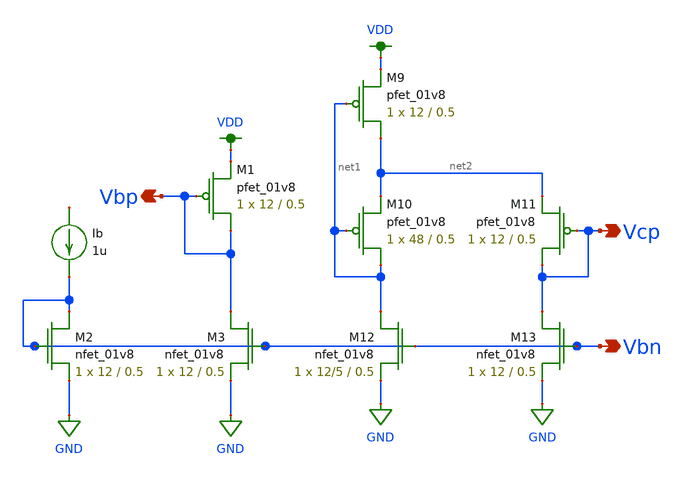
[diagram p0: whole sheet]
** sch_path: simulation/dac/cascode_v_gen.sch
**.subckt cascode_v_gen Vbn Vcp Vbp
*.opin Vbn
*.opin Vcp
*.opin Vbp
XM1 Vbp Vbp VDD VDD sky130_fd_pr__pfet_01v8 L=0.5 W=12 nf=1 ad='int((nf+1)/2) * W/nf * 0.29' as='int((nf+2)/2) * W/nf * 0.29'
+ pd='2*int((nf+1)/2) * (W/nf + 0.29)' ps='2*int((nf+2)/2) * (W/nf + 0.29)' nrd='0.29 / W' nrs='0.29 / W'
+ sa=0 sb=0 sd=0 mult=1 m=1
XM2 Vbn Vbn GND GND sky130_fd_pr__nfet_01v8 L=0.5 W=12 nf=1 ad='int((nf+1)/2) * W/nf * 0.29' as='int((nf+2)/2) * W/nf * 0.29'
+ pd='2*int((nf+1)/2) * (W/nf + 0.29)' ps='2*int((nf+2)/2) * (W/nf + 0.29)' nrd='0.29 / W' nrs='0.29 / W'
+ sa=0 sb=0 sd=0 mult=1 m=1
XM3 Vbp Vbn GND GND sky130_fd_pr__nfet_01v8 L=0.5 W=12 nf=1 ad='int((nf+1)/2) * W/nf * 0.29' as='int((nf+2)/2) * W/nf * 0.29'
+ pd='2*int((nf+1)/2) * (W/nf + 0.29)' ps='2*int((nf+2)/2) * (W/nf + 0.29)' nrd='0.29 / W' nrs='0.29 / W'
+ sa=0 sb=0 sd=0 mult=1 m=1
XM9 net2 net1 VDD VDD sky130_fd_pr__pfet_01v8 L=0.5 W=12 nf=1 ad='int((nf+1)/2) * W/nf * 0.29' as='int((nf+2)/2) * W/nf * 0.29'
+ pd='2*int((nf+1)/2) * (W/nf + 0.29)' ps='2*int((nf+2)/2) * (W/nf + 0.29)' nrd='0.29 / W' nrs='0.29 / W'
+ sa=0 sb=0 sd=0 mult=1 m=1
XM10 net1 net1 net2 VDD sky130_fd_pr__pfet_01v8 L=0.5 W=48 nf=1 ad='int((nf+1)/2) * W/nf * 0.29' as='int((nf+2)/2) * W/nf * 0.29'
+ pd='2*int((nf+1)/2) * (W/nf + 0.29)' ps='2*int((nf+2)/2) * (W/nf + 0.29)' nrd='0.29 / W' nrs='0.29 / W'
+ sa=0 sb=0 sd=0 mult=1 m=1
XM11 Vcp Vcp net2 VDD sky130_fd_pr__pfet_01v8 L=0.5 W=12 nf=1 ad='int((nf+1)/2) * W/nf * 0.29' as='int((nf+2)/2) * W/nf * 0.29'
+ pd='2*int((nf+1)/2) * (W/nf + 0.29)' ps='2*int((nf+2)/2) * (W/nf + 0.29)' nrd='0.29 / W' nrs='0.29 / W'
+ sa=0 sb=0 sd=0 mult=1 m=1
XM12 net1 Vbn GND GND sky130_fd_pr__nfet_01v8 L=0.5 W=12/5 nf=1 ad='int((nf+1)/2) * W/nf * 0.29' as='int((nf+2)/2) * W/nf * 0.29'
+ pd='2*int((nf+1)/2) * (W/nf + 0.29)' ps='2*int((nf+2)/2) * (W/nf + 0.29)' nrd='0.29 / W' nrs='0.29 / W'
+ sa=0 sb=0 sd=0 mult=1 m=1
XM13 Vcp Vbn GND GND sky130_fd_pr__nfet_01v8 L=0.5 W=12 nf=1 ad='int((nf+1)/2) * W/nf * 0.29' as='int((nf+2)/2) * W/nf * 0.29'
+ pd='2*int((nf+1)/2) * (W/nf + 0.29)' ps='2*int((nf+2)/2) * (W/nf + 0.29)' nrd='0.29 / W' nrs='0.29 / W'
+ sa=0 sb=0 sd=0 mult=1 m=1
Ib net3 Vbn 1u
**.ends
.GLOBAL VDD
.GLOBAL GND
.end
